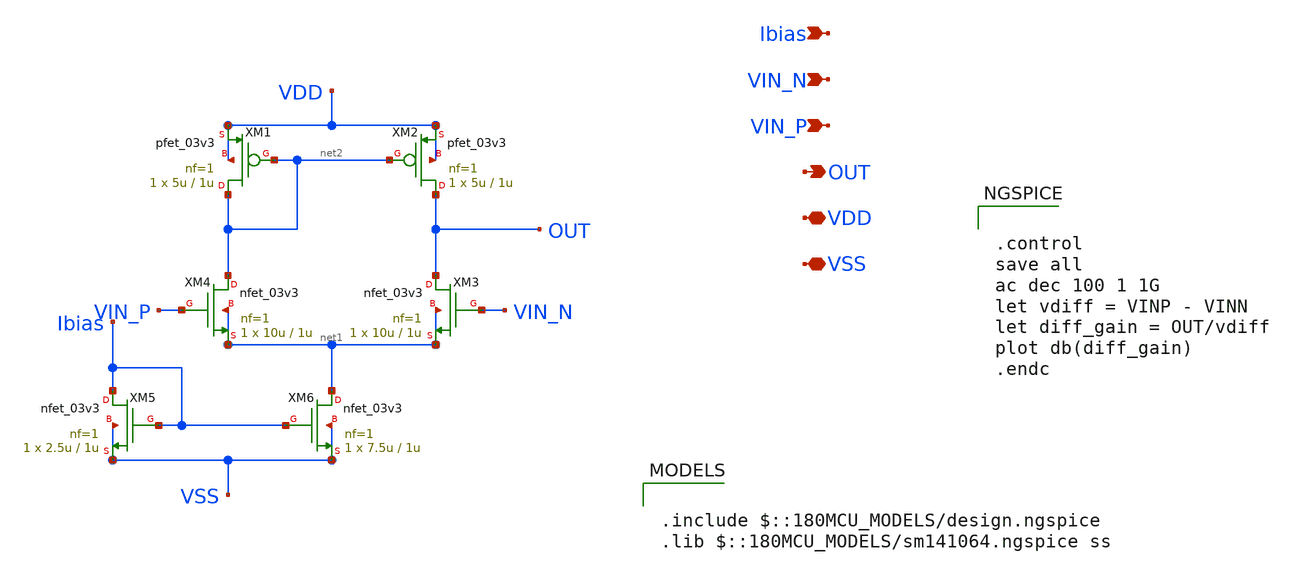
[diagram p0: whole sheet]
** sch_path: week02_current_diffpair/tugas5_cascode_current_mirror/untitled.sch
**.subckt untitled VIN_N VIN_P OUT VDD VSS Ibias
*.ipin VIN_N
*.ipin VIN_P
*.opin OUT
*.iopin VDD
*.iopin VSS
*.ipin Ibias
XM1 net2 net2 VDD VDD pfet_03v3 L=1u W=5u nf=1 ad='int((nf+1)/2) * W/nf * 0.18u' as='int((nf+2)/2) * W/nf * 0.18u'
+ pd='2*int((nf+1)/2) * (W/nf + 0.18u)' ps='2*int((nf+2)/2) * (W/nf + 0.18u)' nrd='0.18u / W' nrs='0.18u / W'
+ sa=0 sb=0 sd=0 m=1
XM2 OUT net2 VDD VDD pfet_03v3 L=1u W=5u nf=1 ad='int((nf+1)/2) * W/nf * 0.18u' as='int((nf+2)/2) * W/nf * 0.18u'
+ pd='2*int((nf+1)/2) * (W/nf + 0.18u)' ps='2*int((nf+2)/2) * (W/nf + 0.18u)' nrd='0.18u / W' nrs='0.18u / W'
+ sa=0 sb=0 sd=0 m=1
XM3 OUT VIN_N net1 net1 nfet_03v3 L=1u W=10u nf=1 ad='int((nf+1)/2) * W/nf * 0.18u' as='int((nf+2)/2) * W/nf * 0.18u'
+ pd='2*int((nf+1)/2) * (W/nf + 0.18u)' ps='2*int((nf+2)/2) * (W/nf + 0.18u)' nrd='0.18u / W' nrs='0.18u / W'
+ sa=0 sb=0 sd=0 m=1
XM4 net2 VIN_P net1 net1 nfet_03v3 L=1u W=10u nf=1 ad='int((nf+1)/2) * W/nf * 0.18u' as='int((nf+2)/2) * W/nf * 0.18u'
+ pd='2*int((nf+1)/2) * (W/nf + 0.18u)' ps='2*int((nf+2)/2) * (W/nf + 0.18u)' nrd='0.18u / W' nrs='0.18u / W'
+ sa=0 sb=0 sd=0 m=1
XM5 Ibias Ibias VSS VSS nfet_03v3 L=1u W=2.5u nf=1 ad='int((nf+1)/2) * W/nf * 0.18u' as='int((nf+2)/2) * W/nf * 0.18u'
+ pd='2*int((nf+1)/2) * (W/nf + 0.18u)' ps='2*int((nf+2)/2) * (W/nf + 0.18u)' nrd='0.18u / W' nrs='0.18u / W'
+ sa=0 sb=0 sd=0 m=1
XM6 net1 Ibias VSS VSS nfet_03v3 L=1u W=7.5u nf=1 ad='int((nf+1)/2) * W/nf * 0.18u' as='int((nf+2)/2) * W/nf * 0.18u'
+ pd='2*int((nf+1)/2) * (W/nf + 0.18u)' ps='2*int((nf+2)/2) * (W/nf + 0.18u)' nrd='0.18u / W' nrs='0.18u / W'
+ sa=0 sb=0 sd=0 m=1
**** begin user architecture code

.include $::180MCU_MODELS/design.ngspice
.lib $::180MCU_MODELS/sm141064.ngspice ss



.control
save all
ac dec 100 1 1G
let vdiff = VINP - VINN
let diff_gain = OUT/vdiff
plot db(diff_gain)
.endc


**** end user architecture code
**.ends
.end
